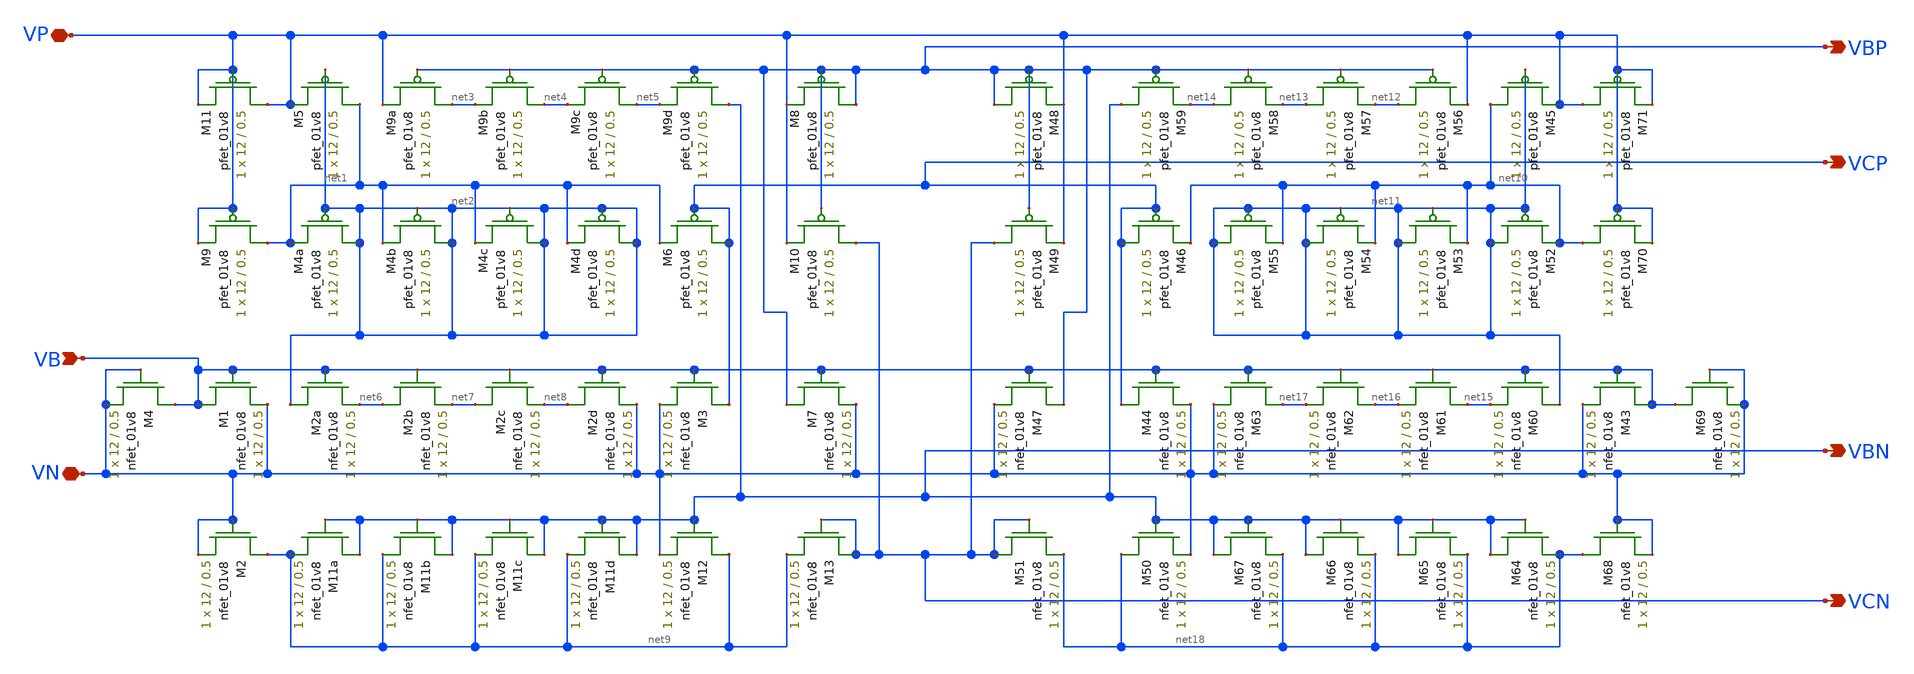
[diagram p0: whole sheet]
** sch_path: mp3/bias_gen/bias_gen_LDS_Final.sch
**.subckt bias_gen_LDS_Final VN VP VCN VCP VBP VB VBN
*.iopin VN
*.iopin VP
*.opin VCN
*.opin VCP
*.opin VBP
*.ipin VB
*.opin VBN
XM1 VB VB VN VN sky130_fd_pr__nfet_01v8 L=0.5 W=12 nf=1 ad='int((nf+1)/2) * W/nf * 0.29' as='int((nf+2)/2) * W/nf * 0.29'
+ pd='2*int((nf+1)/2) * (W/nf + 0.29)' ps='2*int((nf+2)/2) * (W/nf + 0.29)' nrd='0.29 / W' nrs='0.29 / W'
+ sa=0 sb=0 sd=0 mult=1 m=1
XM3 VCP VB VN VN sky130_fd_pr__nfet_01v8 L=0.5 W=12 nf=1 ad='int((nf+1)/2) * W/nf * 0.29' as='int((nf+2)/2) * W/nf * 0.29'
+ pd='2*int((nf+1)/2) * (W/nf + 0.29)' ps='2*int((nf+2)/2) * (W/nf + 0.29)' nrd='0.29 / W' nrs='0.29 / W'
+ sa=0 sb=0 sd=0 mult=1 m=1
XM5 net1 net2 VP VP sky130_fd_pr__pfet_01v8 L=0.5 W=12 nf=1 ad='int((nf+1)/2) * W/nf * 0.29' as='int((nf+2)/2) * W/nf * 0.29'
+ pd='2*int((nf+1)/2) * (W/nf + 0.29)' ps='2*int((nf+2)/2) * (W/nf + 0.29)' nrd='0.29 / W' nrs='0.29 / W'
+ sa=0 sb=0 sd=0 mult=1 m=1
XM6 VCP VCP net1 VP sky130_fd_pr__pfet_01v8 L=0.5 W=12 nf=1 ad='int((nf+1)/2) * W/nf * 0.29' as='int((nf+2)/2) * W/nf * 0.29'
+ pd='2*int((nf+1)/2) * (W/nf + 0.29)' ps='2*int((nf+2)/2) * (W/nf + 0.29)' nrd='0.29 / W' nrs='0.29 / W'
+ sa=0 sb=0 sd=0 mult=1 m=1
XM7 VBP VB VN VN sky130_fd_pr__nfet_01v8 L=0.5 W=12 nf=1 ad='int((nf+1)/2) * W/nf * 0.29' as='int((nf+2)/2) * W/nf * 0.29'
+ pd='2*int((nf+1)/2) * (W/nf + 0.29)' ps='2*int((nf+2)/2) * (W/nf + 0.29)' nrd='0.29 / W' nrs='0.29 / W'
+ sa=0 sb=0 sd=0 mult=1 m=1
XM8 VBP VBP VP VP sky130_fd_pr__pfet_01v8 L=0.5 W=12 nf=1 ad='int((nf+1)/2) * W/nf * 0.29' as='int((nf+2)/2) * W/nf * 0.29'
+ pd='2*int((nf+1)/2) * (W/nf + 0.29)' ps='2*int((nf+2)/2) * (W/nf + 0.29)' nrd='0.29 / W' nrs='0.29 / W'
+ sa=0 sb=0 sd=0 mult=1 m=1
XM10 VCN VBP VP VP sky130_fd_pr__pfet_01v8 L=0.5 W=12 nf=1 ad='int((nf+1)/2) * W/nf * 0.29' as='int((nf+2)/2) * W/nf * 0.29'
+ pd='2*int((nf+1)/2) * (W/nf + 0.29)' ps='2*int((nf+2)/2) * (W/nf + 0.29)' nrd='0.29 / W' nrs='0.29 / W'
+ sa=0 sb=0 sd=0 mult=1 m=1
XM12 net9 VBN VN VN sky130_fd_pr__nfet_01v8 L=0.5 W=12 nf=1 ad='int((nf+1)/2) * W/nf * 0.29' as='int((nf+2)/2) * W/nf * 0.29'
+ pd='2*int((nf+1)/2) * (W/nf + 0.29)' ps='2*int((nf+2)/2) * (W/nf + 0.29)' nrd='0.29 / W' nrs='0.29 / W'
+ sa=0 sb=0 sd=0 mult=1 m=1
XM13 VCN VCN net9 VN sky130_fd_pr__nfet_01v8 L=0.5 W=12 nf=1 ad='int((nf+1)/2) * W/nf * 0.29' as='int((nf+2)/2) * W/nf * 0.29'
+ pd='2*int((nf+1)/2) * (W/nf + 0.29)' ps='2*int((nf+2)/2) * (W/nf + 0.29)' nrd='0.29 / W' nrs='0.29 / W'
+ sa=0 sb=0 sd=0 mult=1 m=1
XM4a net2 net2 net1 VP sky130_fd_pr__pfet_01v8 L=0.5 W=12 nf=1 ad='int((nf+1)/2) * W/nf * 0.29' as='int((nf+2)/2) * W/nf * 0.29'
+ pd='2*int((nf+1)/2) * (W/nf + 0.29)' ps='2*int((nf+2)/2) * (W/nf + 0.29)' nrd='0.29 / W' nrs='0.29 / W'
+ sa=0 sb=0 sd=0 mult=1 m=1
XM4b net2 net2 net1 VP sky130_fd_pr__pfet_01v8 L=0.5 W=12 nf=1 ad='int((nf+1)/2) * W/nf * 0.29' as='int((nf+2)/2) * W/nf * 0.29'
+ pd='2*int((nf+1)/2) * (W/nf + 0.29)' ps='2*int((nf+2)/2) * (W/nf + 0.29)' nrd='0.29 / W' nrs='0.29 / W'
+ sa=0 sb=0 sd=0 mult=1 m=1
XM4c net2 net2 net1 VP sky130_fd_pr__pfet_01v8 L=0.5 W=12 nf=1 ad='int((nf+1)/2) * W/nf * 0.29' as='int((nf+2)/2) * W/nf * 0.29'
+ pd='2*int((nf+1)/2) * (W/nf + 0.29)' ps='2*int((nf+2)/2) * (W/nf + 0.29)' nrd='0.29 / W' nrs='0.29 / W'
+ sa=0 sb=0 sd=0 mult=1 m=1
XM4d net2 net2 net1 VP sky130_fd_pr__pfet_01v8 L=0.5 W=12 nf=1 ad='int((nf+1)/2) * W/nf * 0.29' as='int((nf+2)/2) * W/nf * 0.29'
+ pd='2*int((nf+1)/2) * (W/nf + 0.29)' ps='2*int((nf+2)/2) * (W/nf + 0.29)' nrd='0.29 / W' nrs='0.29 / W'
+ sa=0 sb=0 sd=0 mult=1 m=1
XM9a net3 VBP VP VP sky130_fd_pr__pfet_01v8 L=0.5 W=12 nf=1 ad='int((nf+1)/2) * W/nf * 0.29' as='int((nf+2)/2) * W/nf * 0.29'
+ pd='2*int((nf+1)/2) * (W/nf + 0.29)' ps='2*int((nf+2)/2) * (W/nf + 0.29)' nrd='0.29 / W' nrs='0.29 / W'
+ sa=0 sb=0 sd=0 mult=1 m=1
XM9b net4 VBP net3 VP sky130_fd_pr__pfet_01v8 L=0.5 W=12 nf=1 ad='int((nf+1)/2) * W/nf * 0.29' as='int((nf+2)/2) * W/nf * 0.29'
+ pd='2*int((nf+1)/2) * (W/nf + 0.29)' ps='2*int((nf+2)/2) * (W/nf + 0.29)' nrd='0.29 / W' nrs='0.29 / W'
+ sa=0 sb=0 sd=0 mult=1 m=1
XM9c net5 VBP net4 VP sky130_fd_pr__pfet_01v8 L=0.5 W=12 nf=1 ad='int((nf+1)/2) * W/nf * 0.29' as='int((nf+2)/2) * W/nf * 0.29'
+ pd='2*int((nf+1)/2) * (W/nf + 0.29)' ps='2*int((nf+2)/2) * (W/nf + 0.29)' nrd='0.29 / W' nrs='0.29 / W'
+ sa=0 sb=0 sd=0 mult=1 m=1
XM9d VBN VBP net5 VP sky130_fd_pr__pfet_01v8 L=0.5 W=12 nf=1 ad='int((nf+1)/2) * W/nf * 0.29' as='int((nf+2)/2) * W/nf * 0.29'
+ pd='2*int((nf+1)/2) * (W/nf + 0.29)' ps='2*int((nf+2)/2) * (W/nf + 0.29)' nrd='0.29 / W' nrs='0.29 / W'
+ sa=0 sb=0 sd=0 mult=1 m=1
XM2a net2 VB net6 VN sky130_fd_pr__nfet_01v8 L=0.5 W=12 nf=1 ad='int((nf+1)/2) * W/nf * 0.29' as='int((nf+2)/2) * W/nf * 0.29'
+ pd='2*int((nf+1)/2) * (W/nf + 0.29)' ps='2*int((nf+2)/2) * (W/nf + 0.29)' nrd='0.29 / W' nrs='0.29 / W'
+ sa=0 sb=0 sd=0 mult=1 m=1
XM2b net6 VB net7 VN sky130_fd_pr__nfet_01v8 L=0.5 W=12 nf=1 ad='int((nf+1)/2) * W/nf * 0.29' as='int((nf+2)/2) * W/nf * 0.29'
+ pd='2*int((nf+1)/2) * (W/nf + 0.29)' ps='2*int((nf+2)/2) * (W/nf + 0.29)' nrd='0.29 / W' nrs='0.29 / W'
+ sa=0 sb=0 sd=0 mult=1 m=1
XM2c net7 VB net8 VN sky130_fd_pr__nfet_01v8 L=0.5 W=12 nf=1 ad='int((nf+1)/2) * W/nf * 0.29' as='int((nf+2)/2) * W/nf * 0.29'
+ pd='2*int((nf+1)/2) * (W/nf + 0.29)' ps='2*int((nf+2)/2) * (W/nf + 0.29)' nrd='0.29 / W' nrs='0.29 / W'
+ sa=0 sb=0 sd=0 mult=1 m=1
XM2d net8 VB VN VN sky130_fd_pr__nfet_01v8 L=0.5 W=12 nf=1 ad='int((nf+1)/2) * W/nf * 0.29' as='int((nf+2)/2) * W/nf * 0.29'
+ pd='2*int((nf+1)/2) * (W/nf + 0.29)' ps='2*int((nf+2)/2) * (W/nf + 0.29)' nrd='0.29 / W' nrs='0.29 / W'
+ sa=0 sb=0 sd=0 mult=1 m=1
XM11a VBN VBN net9 VN sky130_fd_pr__nfet_01v8 L=0.5 W=12 nf=1 ad='int((nf+1)/2) * W/nf * 0.29' as='int((nf+2)/2) * W/nf * 0.29'
+ pd='2*int((nf+1)/2) * (W/nf + 0.29)' ps='2*int((nf+2)/2) * (W/nf + 0.29)' nrd='0.29 / W' nrs='0.29 / W'
+ sa=0 sb=0 sd=0 mult=1 m=1
XM11b VBN VBN net9 VN sky130_fd_pr__nfet_01v8 L=0.5 W=12 nf=1 ad='int((nf+1)/2) * W/nf * 0.29' as='int((nf+2)/2) * W/nf * 0.29'
+ pd='2*int((nf+1)/2) * (W/nf + 0.29)' ps='2*int((nf+2)/2) * (W/nf + 0.29)' nrd='0.29 / W' nrs='0.29 / W'
+ sa=0 sb=0 sd=0 mult=1 m=1
XM11c VBN VBN net9 VN sky130_fd_pr__nfet_01v8 L=0.5 W=12 nf=1 ad='int((nf+1)/2) * W/nf * 0.29' as='int((nf+2)/2) * W/nf * 0.29'
+ pd='2*int((nf+1)/2) * (W/nf + 0.29)' ps='2*int((nf+2)/2) * (W/nf + 0.29)' nrd='0.29 / W' nrs='0.29 / W'
+ sa=0 sb=0 sd=0 mult=1 m=1
XM11d VBN VBN net9 VN sky130_fd_pr__nfet_01v8 L=0.5 W=12 nf=1 ad='int((nf+1)/2) * W/nf * 0.29' as='int((nf+2)/2) * W/nf * 0.29'
+ pd='2*int((nf+1)/2) * (W/nf + 0.29)' ps='2*int((nf+2)/2) * (W/nf + 0.29)' nrd='0.29 / W' nrs='0.29 / W'
+ sa=0 sb=0 sd=0 mult=1 m=1
XM2 net9 VN VN VN sky130_fd_pr__nfet_01v8 L=0.5 W=12 nf=1 ad='int((nf+1)/2) * W/nf * 0.29' as='int((nf+2)/2) * W/nf * 0.29'
+ pd='2*int((nf+1)/2) * (W/nf + 0.29)' ps='2*int((nf+2)/2) * (W/nf + 0.29)' nrd='0.29 / W' nrs='0.29 / W'
+ sa=0 sb=0 sd=0 mult=1 m=1
XM4 VB VN VN VN sky130_fd_pr__nfet_01v8 L=0.5 W=12 nf=1 ad='int((nf+1)/2) * W/nf * 0.29' as='int((nf+2)/2) * W/nf * 0.29'
+ pd='2*int((nf+1)/2) * (W/nf + 0.29)' ps='2*int((nf+2)/2) * (W/nf + 0.29)' nrd='0.29 / W' nrs='0.29 / W'
+ sa=0 sb=0 sd=0 mult=1 m=1
XM9 net1 VP VP VP sky130_fd_pr__pfet_01v8 L=0.5 W=12 nf=1 ad='int((nf+1)/2) * W/nf * 0.29' as='int((nf+2)/2) * W/nf * 0.29'
+ pd='2*int((nf+1)/2) * (W/nf + 0.29)' ps='2*int((nf+2)/2) * (W/nf + 0.29)' nrd='0.29 / W' nrs='0.29 / W'
+ sa=0 sb=0 sd=0 mult=1 m=1
XM11 VP VP VP VP sky130_fd_pr__pfet_01v8 L=0.5 W=12 nf=1 ad='int((nf+1)/2) * W/nf * 0.29' as='int((nf+2)/2) * W/nf * 0.29'
+ pd='2*int((nf+1)/2) * (W/nf + 0.29)' ps='2*int((nf+2)/2) * (W/nf + 0.29)' nrd='0.29 / W' nrs='0.29 / W'
+ sa=0 sb=0 sd=0 mult=1 m=1
XM43 VB VB VN VN sky130_fd_pr__nfet_01v8 L=0.5 W=12 nf=1 ad='int((nf+1)/2) * W/nf * 0.29' as='int((nf+2)/2) * W/nf * 0.29'
+ pd='2*int((nf+1)/2) * (W/nf + 0.29)' ps='2*int((nf+2)/2) * (W/nf + 0.29)' nrd='0.29 / W' nrs='0.29 / W'
+ sa=0 sb=0 sd=0 mult=1 m=1
XM44 VCP VB VN VN sky130_fd_pr__nfet_01v8 L=0.5 W=12 nf=1 ad='int((nf+1)/2) * W/nf * 0.29' as='int((nf+2)/2) * W/nf * 0.29'
+ pd='2*int((nf+1)/2) * (W/nf + 0.29)' ps='2*int((nf+2)/2) * (W/nf + 0.29)' nrd='0.29 / W' nrs='0.29 / W'
+ sa=0 sb=0 sd=0 mult=1 m=1
XM45 net10 net11 VP VP sky130_fd_pr__pfet_01v8 L=0.5 W=12 nf=1 ad='int((nf+1)/2) * W/nf * 0.29' as='int((nf+2)/2) * W/nf * 0.29'
+ pd='2*int((nf+1)/2) * (W/nf + 0.29)' ps='2*int((nf+2)/2) * (W/nf + 0.29)' nrd='0.29 / W' nrs='0.29 / W'
+ sa=0 sb=0 sd=0 mult=1 m=1
XM46 VCP VCP net10 VP sky130_fd_pr__pfet_01v8 L=0.5 W=12 nf=1 ad='int((nf+1)/2) * W/nf * 0.29' as='int((nf+2)/2) * W/nf * 0.29'
+ pd='2*int((nf+1)/2) * (W/nf + 0.29)' ps='2*int((nf+2)/2) * (W/nf + 0.29)' nrd='0.29 / W' nrs='0.29 / W'
+ sa=0 sb=0 sd=0 mult=1 m=1
XM47 VBP VB VN VN sky130_fd_pr__nfet_01v8 L=0.5 W=12 nf=1 ad='int((nf+1)/2) * W/nf * 0.29' as='int((nf+2)/2) * W/nf * 0.29'
+ pd='2*int((nf+1)/2) * (W/nf + 0.29)' ps='2*int((nf+2)/2) * (W/nf + 0.29)' nrd='0.29 / W' nrs='0.29 / W'
+ sa=0 sb=0 sd=0 mult=1 m=1
XM48 VBP VBP VP VP sky130_fd_pr__pfet_01v8 L=0.5 W=12 nf=1 ad='int((nf+1)/2) * W/nf * 0.29' as='int((nf+2)/2) * W/nf * 0.29'
+ pd='2*int((nf+1)/2) * (W/nf + 0.29)' ps='2*int((nf+2)/2) * (W/nf + 0.29)' nrd='0.29 / W' nrs='0.29 / W'
+ sa=0 sb=0 sd=0 mult=1 m=1
XM49 VCN VBP VP VP sky130_fd_pr__pfet_01v8 L=0.5 W=12 nf=1 ad='int((nf+1)/2) * W/nf * 0.29' as='int((nf+2)/2) * W/nf * 0.29'
+ pd='2*int((nf+1)/2) * (W/nf + 0.29)' ps='2*int((nf+2)/2) * (W/nf + 0.29)' nrd='0.29 / W' nrs='0.29 / W'
+ sa=0 sb=0 sd=0 mult=1 m=1
XM50 net18 VBN VN VN sky130_fd_pr__nfet_01v8 L=0.5 W=12 nf=1 ad='int((nf+1)/2) * W/nf * 0.29' as='int((nf+2)/2) * W/nf * 0.29'
+ pd='2*int((nf+1)/2) * (W/nf + 0.29)' ps='2*int((nf+2)/2) * (W/nf + 0.29)' nrd='0.29 / W' nrs='0.29 / W'
+ sa=0 sb=0 sd=0 mult=1 m=1
XM51 VCN VCN net18 VN sky130_fd_pr__nfet_01v8 L=0.5 W=12 nf=1 ad='int((nf+1)/2) * W/nf * 0.29' as='int((nf+2)/2) * W/nf * 0.29'
+ pd='2*int((nf+1)/2) * (W/nf + 0.29)' ps='2*int((nf+2)/2) * (W/nf + 0.29)' nrd='0.29 / W' nrs='0.29 / W'
+ sa=0 sb=0 sd=0 mult=1 m=1
XM52 net11 net11 net10 VP sky130_fd_pr__pfet_01v8 L=0.5 W=12 nf=1 ad='int((nf+1)/2) * W/nf * 0.29' as='int((nf+2)/2) * W/nf * 0.29'
+ pd='2*int((nf+1)/2) * (W/nf + 0.29)' ps='2*int((nf+2)/2) * (W/nf + 0.29)' nrd='0.29 / W' nrs='0.29 / W'
+ sa=0 sb=0 sd=0 mult=1 m=1
XM53 net11 net11 net10 VP sky130_fd_pr__pfet_01v8 L=0.5 W=12 nf=1 ad='int((nf+1)/2) * W/nf * 0.29' as='int((nf+2)/2) * W/nf * 0.29'
+ pd='2*int((nf+1)/2) * (W/nf + 0.29)' ps='2*int((nf+2)/2) * (W/nf + 0.29)' nrd='0.29 / W' nrs='0.29 / W'
+ sa=0 sb=0 sd=0 mult=1 m=1
XM54 net11 net11 net10 VP sky130_fd_pr__pfet_01v8 L=0.5 W=12 nf=1 ad='int((nf+1)/2) * W/nf * 0.29' as='int((nf+2)/2) * W/nf * 0.29'
+ pd='2*int((nf+1)/2) * (W/nf + 0.29)' ps='2*int((nf+2)/2) * (W/nf + 0.29)' nrd='0.29 / W' nrs='0.29 / W'
+ sa=0 sb=0 sd=0 mult=1 m=1
XM55 net11 net11 net10 VP sky130_fd_pr__pfet_01v8 L=0.5 W=12 nf=1 ad='int((nf+1)/2) * W/nf * 0.29' as='int((nf+2)/2) * W/nf * 0.29'
+ pd='2*int((nf+1)/2) * (W/nf + 0.29)' ps='2*int((nf+2)/2) * (W/nf + 0.29)' nrd='0.29 / W' nrs='0.29 / W'
+ sa=0 sb=0 sd=0 mult=1 m=1
XM56 net12 VBP VP VP sky130_fd_pr__pfet_01v8 L=0.5 W=12 nf=1 ad='int((nf+1)/2) * W/nf * 0.29' as='int((nf+2)/2) * W/nf * 0.29'
+ pd='2*int((nf+1)/2) * (W/nf + 0.29)' ps='2*int((nf+2)/2) * (W/nf + 0.29)' nrd='0.29 / W' nrs='0.29 / W'
+ sa=0 sb=0 sd=0 mult=1 m=1
XM57 net13 VBP net12 VP sky130_fd_pr__pfet_01v8 L=0.5 W=12 nf=1 ad='int((nf+1)/2) * W/nf * 0.29' as='int((nf+2)/2) * W/nf * 0.29'
+ pd='2*int((nf+1)/2) * (W/nf + 0.29)' ps='2*int((nf+2)/2) * (W/nf + 0.29)' nrd='0.29 / W' nrs='0.29 / W'
+ sa=0 sb=0 sd=0 mult=1 m=1
XM58 net14 VBP net13 VP sky130_fd_pr__pfet_01v8 L=0.5 W=12 nf=1 ad='int((nf+1)/2) * W/nf * 0.29' as='int((nf+2)/2) * W/nf * 0.29'
+ pd='2*int((nf+1)/2) * (W/nf + 0.29)' ps='2*int((nf+2)/2) * (W/nf + 0.29)' nrd='0.29 / W' nrs='0.29 / W'
+ sa=0 sb=0 sd=0 mult=1 m=1
XM59 VBN VBP net14 VP sky130_fd_pr__pfet_01v8 L=0.5 W=12 nf=1 ad='int((nf+1)/2) * W/nf * 0.29' as='int((nf+2)/2) * W/nf * 0.29'
+ pd='2*int((nf+1)/2) * (W/nf + 0.29)' ps='2*int((nf+2)/2) * (W/nf + 0.29)' nrd='0.29 / W' nrs='0.29 / W'
+ sa=0 sb=0 sd=0 mult=1 m=1
XM60 net11 VB net15 VN sky130_fd_pr__nfet_01v8 L=0.5 W=12 nf=1 ad='int((nf+1)/2) * W/nf * 0.29' as='int((nf+2)/2) * W/nf * 0.29'
+ pd='2*int((nf+1)/2) * (W/nf + 0.29)' ps='2*int((nf+2)/2) * (W/nf + 0.29)' nrd='0.29 / W' nrs='0.29 / W'
+ sa=0 sb=0 sd=0 mult=1 m=1
XM61 net15 VB net16 VN sky130_fd_pr__nfet_01v8 L=0.5 W=12 nf=1 ad='int((nf+1)/2) * W/nf * 0.29' as='int((nf+2)/2) * W/nf * 0.29'
+ pd='2*int((nf+1)/2) * (W/nf + 0.29)' ps='2*int((nf+2)/2) * (W/nf + 0.29)' nrd='0.29 / W' nrs='0.29 / W'
+ sa=0 sb=0 sd=0 mult=1 m=1
XM62 net16 VB net17 VN sky130_fd_pr__nfet_01v8 L=0.5 W=12 nf=1 ad='int((nf+1)/2) * W/nf * 0.29' as='int((nf+2)/2) * W/nf * 0.29'
+ pd='2*int((nf+1)/2) * (W/nf + 0.29)' ps='2*int((nf+2)/2) * (W/nf + 0.29)' nrd='0.29 / W' nrs='0.29 / W'
+ sa=0 sb=0 sd=0 mult=1 m=1
XM63 net17 VB VN VN sky130_fd_pr__nfet_01v8 L=0.5 W=12 nf=1 ad='int((nf+1)/2) * W/nf * 0.29' as='int((nf+2)/2) * W/nf * 0.29'
+ pd='2*int((nf+1)/2) * (W/nf + 0.29)' ps='2*int((nf+2)/2) * (W/nf + 0.29)' nrd='0.29 / W' nrs='0.29 / W'
+ sa=0 sb=0 sd=0 mult=1 m=1
XM64 VBN VBN net18 VN sky130_fd_pr__nfet_01v8 L=0.5 W=12 nf=1 ad='int((nf+1)/2) * W/nf * 0.29' as='int((nf+2)/2) * W/nf * 0.29'
+ pd='2*int((nf+1)/2) * (W/nf + 0.29)' ps='2*int((nf+2)/2) * (W/nf + 0.29)' nrd='0.29 / W' nrs='0.29 / W'
+ sa=0 sb=0 sd=0 mult=1 m=1
XM65 VBN VBN net18 VN sky130_fd_pr__nfet_01v8 L=0.5 W=12 nf=1 ad='int((nf+1)/2) * W/nf * 0.29' as='int((nf+2)/2) * W/nf * 0.29'
+ pd='2*int((nf+1)/2) * (W/nf + 0.29)' ps='2*int((nf+2)/2) * (W/nf + 0.29)' nrd='0.29 / W' nrs='0.29 / W'
+ sa=0 sb=0 sd=0 mult=1 m=1
XM66 VBN VBN net18 VN sky130_fd_pr__nfet_01v8 L=0.5 W=12 nf=1 ad='int((nf+1)/2) * W/nf * 0.29' as='int((nf+2)/2) * W/nf * 0.29'
+ pd='2*int((nf+1)/2) * (W/nf + 0.29)' ps='2*int((nf+2)/2) * (W/nf + 0.29)' nrd='0.29 / W' nrs='0.29 / W'
+ sa=0 sb=0 sd=0 mult=1 m=1
XM67 VBN VBN net18 VN sky130_fd_pr__nfet_01v8 L=0.5 W=12 nf=1 ad='int((nf+1)/2) * W/nf * 0.29' as='int((nf+2)/2) * W/nf * 0.29'
+ pd='2*int((nf+1)/2) * (W/nf + 0.29)' ps='2*int((nf+2)/2) * (W/nf + 0.29)' nrd='0.29 / W' nrs='0.29 / W'
+ sa=0 sb=0 sd=0 mult=1 m=1
XM68 net18 VN VN VN sky130_fd_pr__nfet_01v8 L=0.5 W=12 nf=1 ad='int((nf+1)/2) * W/nf * 0.29' as='int((nf+2)/2) * W/nf * 0.29'
+ pd='2*int((nf+1)/2) * (W/nf + 0.29)' ps='2*int((nf+2)/2) * (W/nf + 0.29)' nrd='0.29 / W' nrs='0.29 / W'
+ sa=0 sb=0 sd=0 mult=1 m=1
XM69 VB VN VN VN sky130_fd_pr__nfet_01v8 L=0.5 W=12 nf=1 ad='int((nf+1)/2) * W/nf * 0.29' as='int((nf+2)/2) * W/nf * 0.29'
+ pd='2*int((nf+1)/2) * (W/nf + 0.29)' ps='2*int((nf+2)/2) * (W/nf + 0.29)' nrd='0.29 / W' nrs='0.29 / W'
+ sa=0 sb=0 sd=0 mult=1 m=1
XM70 net10 VP VP VP sky130_fd_pr__pfet_01v8 L=0.5 W=12 nf=1 ad='int((nf+1)/2) * W/nf * 0.29' as='int((nf+2)/2) * W/nf * 0.29'
+ pd='2*int((nf+1)/2) * (W/nf + 0.29)' ps='2*int((nf+2)/2) * (W/nf + 0.29)' nrd='0.29 / W' nrs='0.29 / W'
+ sa=0 sb=0 sd=0 mult=1 m=1
XM71 VP VP VP VP sky130_fd_pr__pfet_01v8 L=0.5 W=12 nf=1 ad='int((nf+1)/2) * W/nf * 0.29' as='int((nf+2)/2) * W/nf * 0.29'
+ pd='2*int((nf+1)/2) * (W/nf + 0.29)' ps='2*int((nf+2)/2) * (W/nf + 0.29)' nrd='0.29 / W' nrs='0.29 / W'
+ sa=0 sb=0 sd=0 mult=1 m=1
**.ends
.end
